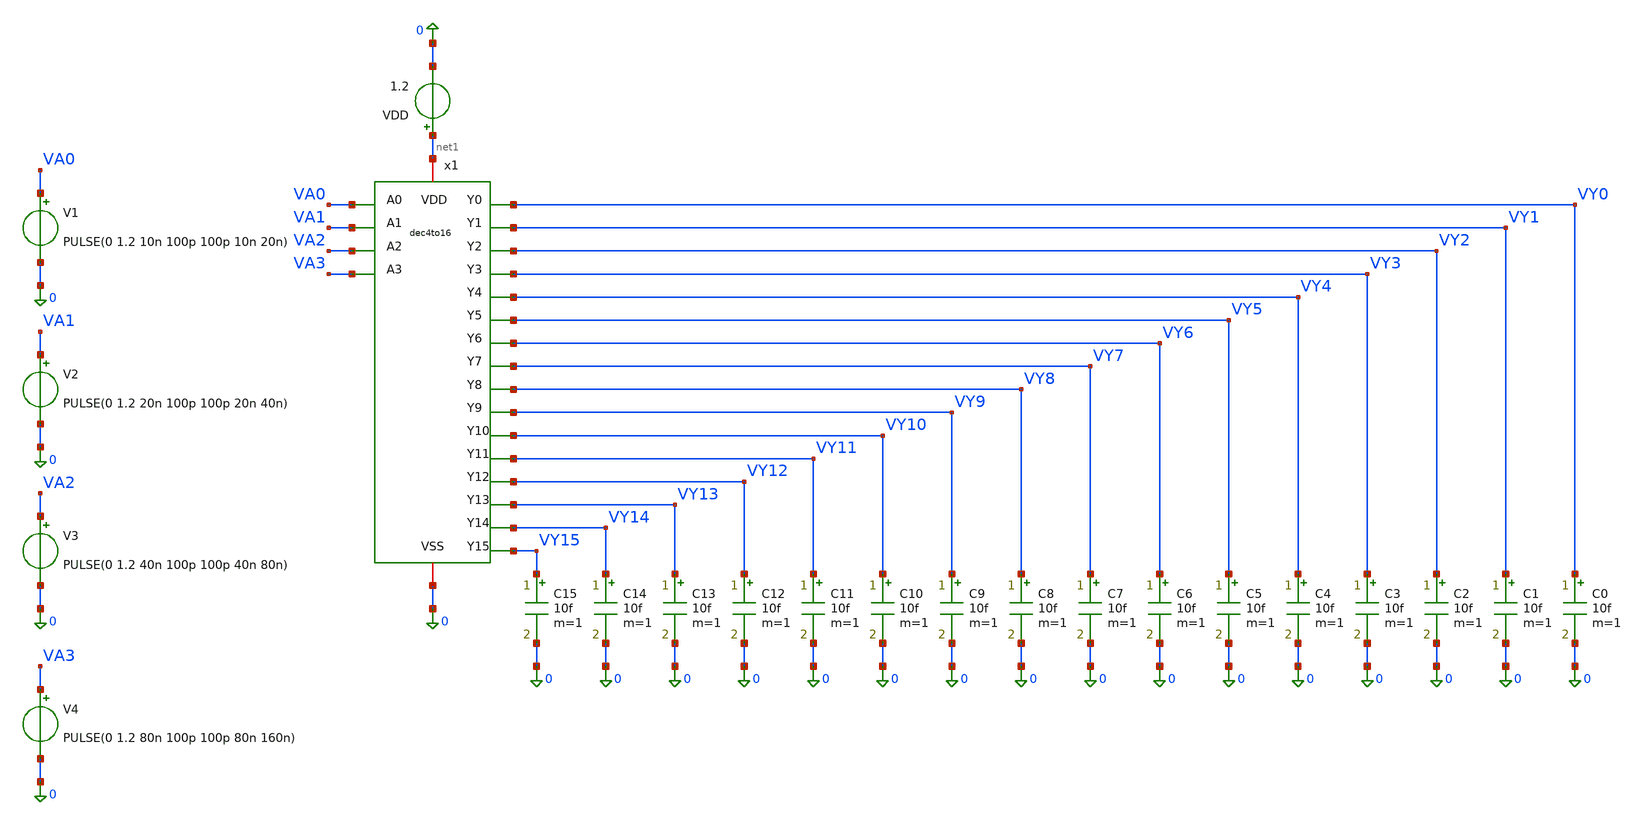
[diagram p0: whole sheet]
** sch_path: designs/libs/core_digital/dec4to16/tb_dec4to16.sch
**.subckt tb_dec4to16
x1 VA0 VA3 VY0 VY1 VY2 VY3 net1 0 VY4 VY5 VY6 VY7 VY8 VY9 VY10 VY11 VY12 VY13 VY14 VY15 VA1 VA2
+ dec4to16
V1 VA0 0 PULSE(0 1.2 10n 100p 100p 10n 20n)
V2 VA1 0 PULSE(0 1.2 20n 100p 100p 20n 40n)
V3 VA2 0 PULSE(0 1.2 40n 100p 100p 40n 80n)
V4 VA3 0 PULSE(0 1.2 80n 100p 100p 80n 160n)
VDD net1 0 1.2
C15 VY15 0 10f m=1
C14 VY14 0 10f m=1
C13 VY13 0 10f m=1
C12 VY12 0 10f m=1
C11 VY11 0 10f m=1
C10 VY10 0 10f m=1
C9 VY9 0 10f m=1
C8 VY8 0 10f m=1
C7 VY7 0 10f m=1
C0 VY0 0 10f m=1
C1 VY1 0 10f m=1
C2 VY2 0 10f m=1
C3 VY3 0 10f m=1
C4 VY4 0 10f m=1
C5 VY5 0 10f m=1
C6 VY6 0 10f m=1
**** begin user architecture code

.lib cornerMOSlv.lib mos_tt
.include /foss/pdks/ihp-sg13cmos5l/libs.ref/sg13cmos5l_stdcell/spice/sg13cmos5l_stdcell.spice


.control
  tran 100p 160n
  write tb_dec4to16.raw

  * ==========================================
  * AUTOMATED TRUTH TABLE VOLTAGE MEASUREMENTS
  * (Each state is sampled at its mid-window)
  * ==========================================
  meas tran v_y0_0000  find v(VY0)  at=5n
  meas tran v_y1_0001  find v(VY1)  at=15n
  meas tran v_y2_0010  find v(VY2)  at=25n
  meas tran v_y3_0011  find v(VY3)  at=35n
  meas tran v_y4_0100  find v(VY4)  at=45n
  meas tran v_y5_0101  find v(VY5)  at=55n
  meas tran v_y6_0110  find v(VY6)  at=65n
  meas tran v_y7_0111  find v(VY7)  at=75n
  meas tran v_y8_1000  find v(VY8)  at=85n
  meas tran v_y9_1001  find v(VY9)  at=95n
  meas tran v_y10_1010 find v(VY10) at=105n
  meas tran v_y11_1011 find v(VY11) at=115n
  meas tran v_y12_1100 find v(VY12) at=125n
  meas tran v_y13_1101 find v(VY13) at=135n
  meas tran v_y14_1110 find v(VY14) at=145n
  meas tran v_y15_1111 find v(VY15) at=155n

  * ==========================================
  * MULTI-TRACE OFFSET PLOTS
  * ==========================================
  * 1. 4-bit Binary Input Code (A0..A3)
  plot v(VA0) v(VA1)+1.5 v(VA2)+3.0 v(VA3)+4.5 title 'Decoder Inputs (A0, A1, A2, A3)' xlabel 'Time (s)'
+ ylabel 'Voltage (V)'

  * 2. Lower 8 Decoded Channels (Y0..Y7)
  plot v(VY0) v(VY1)+1.5 v(VY2)+3.0 v(VY3)+4.5 v(VY4)+6.0 v(VY5)+7.5 v(VY6)+9.0 v(VY7)+10.5 title 'Decoded Outputs (Y0..Y7)'
+ xlabel 'Time (s)' ylabel 'Voltage (V)'

  * 3. Upper 8 Decoded Channels (Y8..Y15)
  plot v(VY8) v(VY9)+1.5 v(VY10)+3.0 v(VY11)+4.5 v(VY12)+6.0 v(VY13)+7.5 v(VY14)+9.0 v(VY15)+10.5 title
+ 'Decoded Outputs (Y8..Y15)' xlabel 'Time (s)' ylabel 'Voltage (V)'
.endc


**** end user architecture code
**.ends

* expanding   symbol:  dec4to16.sym # of pins=22
** sym_path: dec4to16.sym
** sch_path: dec4to16.sch
.subckt dec4to16 A0 A3 Y0 Y1 Y2 Y3 VDD VSS Y4 Y5 Y6 Y7 Y8 Y9 Y10 Y11 Y12 Y13 Y14 Y15 A1 A2
*.ipin A0
*.ipin A1
*.ipin A2
*.ipin A3
*.iopin VDD
*.iopin VSS
*.opin Y0
*.opin Y1
*.opin Y2
*.opin Y3
*.opin Y4
*.opin Y5
*.opin Y6
*.opin Y7
*.opin Y8
*.opin Y9
*.opin Y10
*.opin Y11
*.opin Y12
*.opin Y13
*.opin Y14
*.opin Y15
x_dec_low A0 A1 P0 P1 P2 P3 VDD VSS dec2to4
x_dec_high A2 A3 Q0 Q1 Q2 Q3 VDD VSS dec2to4
x1 Y0 P0 Q0 VDD VSS sg13cmos5l_and2_1
x2 Y4 P0 Q1 VDD VSS sg13cmos5l_and2_1
x3 Y8 P0 Q2 VDD VSS sg13cmos5l_and2_1
x4 Y12 P0 Q3 VDD VSS sg13cmos5l_and2_1
x5 Y1 P1 Q0 VDD VSS sg13cmos5l_and2_1
x6 Y5 P1 Q1 VDD VSS sg13cmos5l_and2_1
x7 Y9 P1 Q2 VDD VSS sg13cmos5l_and2_1
x8 Y13 P1 Q3 VDD VSS sg13cmos5l_and2_1
x9 Y2 P2 Q0 VDD VSS sg13cmos5l_and2_1
x10 Y6 P2 Q1 VDD VSS sg13cmos5l_and2_1
x11 Y10 P2 Q2 VDD VSS sg13cmos5l_and2_1
x12 Y14 P2 Q3 VDD VSS sg13cmos5l_and2_1
x13 Y3 P3 Q0 VDD VSS sg13cmos5l_and2_1
x14 Y7 P3 Q1 VDD VSS sg13cmos5l_and2_1
x15 Y11 P3 Q2 VDD VSS sg13cmos5l_and2_1
x16 Y15 P3 Q3 VDD VSS sg13cmos5l_and2_1
.ends


* expanding   symbol:
*+  /foss/designs/Chipalooza/Programmable-Instrumentation-Amplifier-IP/designs/libs/core_digital/dec2to4/dec2to4.sym # of pins=8
** sym_path: /foss/designs/Chipalooza/Programmable-Instrumentation-Amplifier-IP/designs/libs/core_digital/dec2to4/dec2to4.sym
** sch_path: /foss/designs/Chipalooza/Programmable-Instrumentation-Amplifier-IP/designs/libs/core_digital/dec2to4/dec2to4.sch
.subckt dec2to4 A0 A1 Y0 Y1 Y2 Y3 VDD VSS
*.ipin A0
*.ipin A1
*.opin Y0
*.opin Y1
*.opin Y2
*.opin Y3
*.iopin VDD
*.iopin VSS
x1 net2 A0 VDD VSS sg13cmos5l_inv_1
x2 net1 A1 VDD VSS sg13cmos5l_inv_1
x11 Y0 net2 net1 VDD VSS sg13cmos5l_and2_1
x3 Y1 A0 net1 VDD VSS sg13cmos5l_and2_1
x4 Y2 A1 net2 VDD VSS sg13cmos5l_and2_1
x5 Y3 A1 A0 VDD VSS sg13cmos5l_and2_1
.ends

.end
